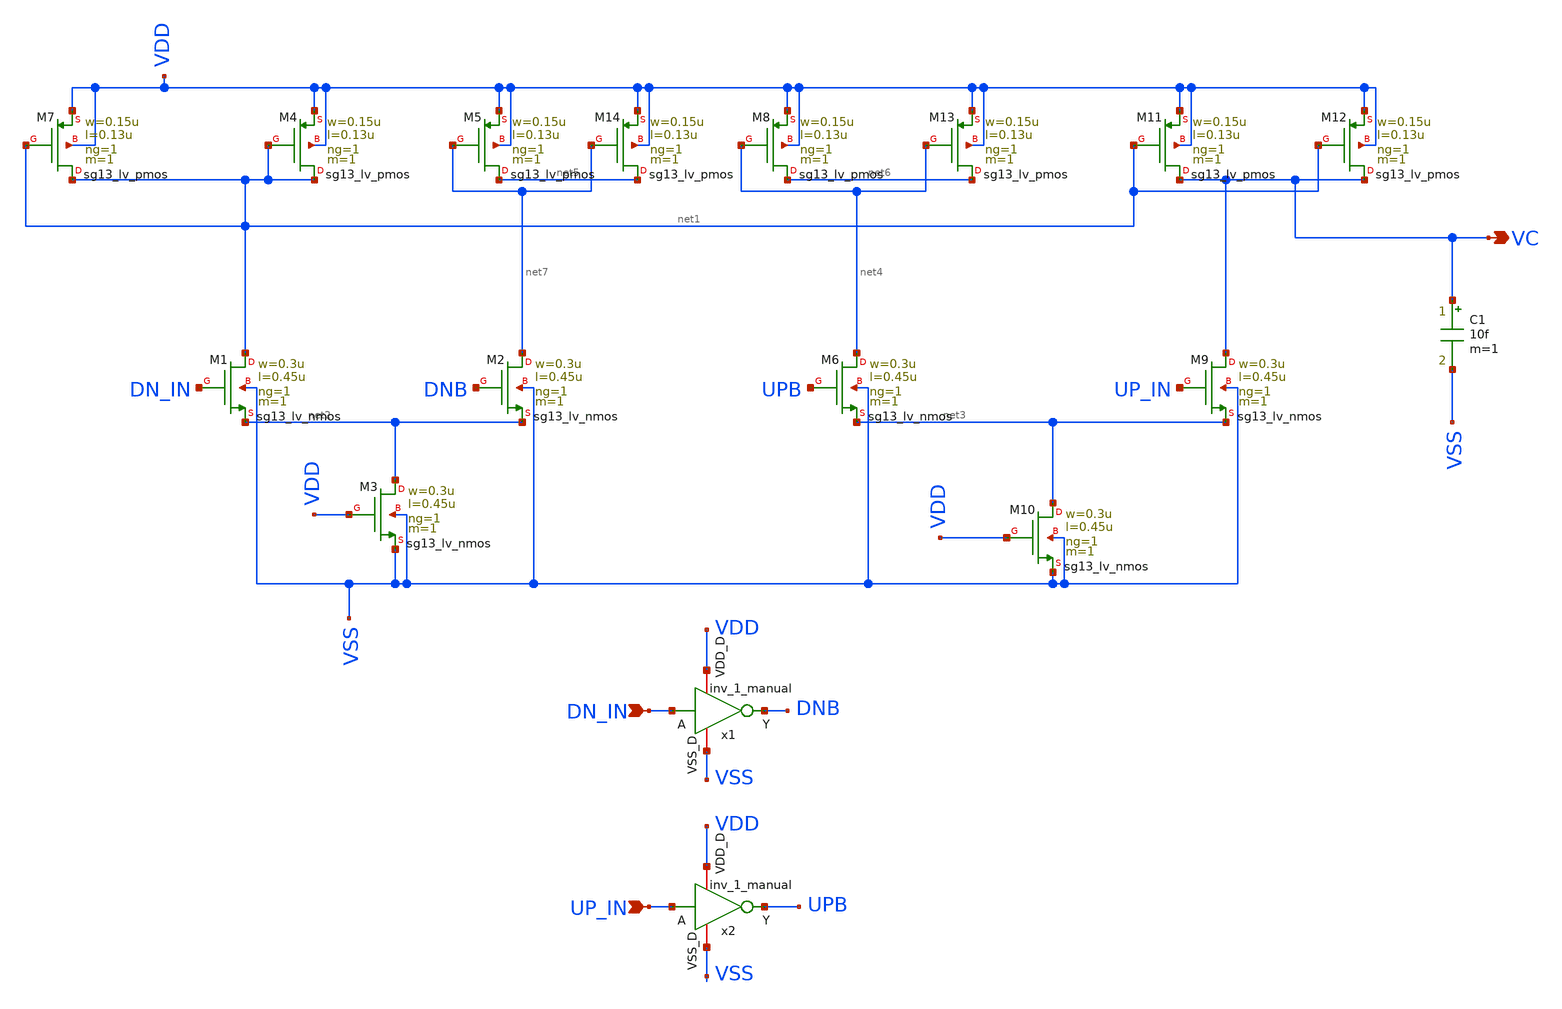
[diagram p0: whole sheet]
** sch_path: sch/push_pull/push_pull.sch
**.subckt push_pull DN_IN UP_IN VC
*.ipin DN_IN
*.ipin UP_IN
*.opin VC
XM1 net1 DN_IN net2 VSS sg13_lv_nmos w=0.3u l=0.45u ng=1 m=1 mm_ok=1
XM7 net1 net1 VDD VDD sg13_lv_pmos w=0.15u l=0.13u ng=1 m=1 mm_ok=1
XM2 net7 DNB net2 VSS sg13_lv_nmos w=0.3u l=0.45u ng=1 m=1 mm_ok=1
XM3 net2 VDD VSS VSS sg13_lv_nmos w=0.3u l=0.45u ng=1 m=1 mm_ok=1
XM4 net1 net1 VDD VDD sg13_lv_pmos w=0.15u l=0.13u ng=1 m=1 mm_ok=1
XM5 net5 net7 VDD VDD sg13_lv_pmos w=0.15u l=0.13u ng=1 m=1 mm_ok=1
XM6 net4 UPB net3 VSS sg13_lv_nmos w=0.3u l=0.45u ng=1 m=1 mm_ok=1
XM8 net6 net4 VDD VDD sg13_lv_pmos w=0.15u l=0.13u ng=1 m=1 mm_ok=1
XM9 VC UP_IN net3 VSS sg13_lv_nmos w=0.3u l=0.45u ng=1 m=1 mm_ok=1
XM10 net3 VDD VSS VSS sg13_lv_nmos w=0.3u l=0.45u ng=1 m=1 mm_ok=1
XM11 VC net1 VDD VDD sg13_lv_pmos w=0.15u l=0.13u ng=1 m=1 mm_ok=1
XM12 VC net1 VDD VDD sg13_lv_pmos w=0.15u l=0.13u ng=1 m=1 mm_ok=1
XM13 net6 net4 VDD VDD sg13_lv_pmos w=0.15u l=0.13u ng=1 m=1 mm_ok=1
XM14 net5 net7 VDD VDD sg13_lv_pmos w=0.15u l=0.13u ng=1 m=1 mm_ok=1
x1 VDD DN_IN DNB VSS inv_1_manual
x2 VDD UP_IN UPB VSS inv_1_manual
C1 VC VSS 10f m=1
**.ends
.end
